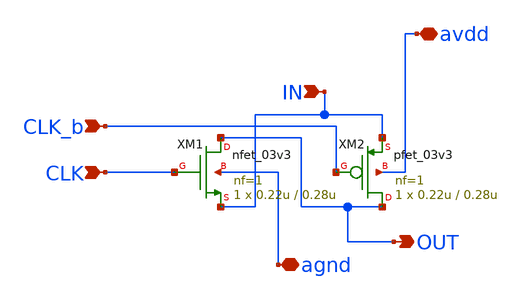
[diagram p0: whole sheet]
** sch_path: mpw18h1/cisar-gen/xschem/TBD/transimission_gate.sch
**.subckt transimission_gate IN OUT avdd agnd CLK_b CLK
*.ipin IN
*.opin OUT
*.iopin avdd
*.iopin agnd
*.ipin CLK_b
*.ipin CLK
XM1 OUT CLK IN agnd nfet_03v3 L=0.28u W=0.22u nf=1 ad='int((nf+1)/2) * W/nf * 0.18u' as='int((nf+2)/2) * W/nf * 0.18u'
+ pd='2*int((nf+1)/2) * (W/nf + 0.18u)' ps='2*int((nf+2)/2) * (W/nf + 0.18u)' nrd='0.18u / W' nrs='0.18u / W'
+ sa=0 sb=0 sd=0 m=1
XM2 OUT CLK_b IN avdd pfet_03v3 L=0.28u W=0.22u nf=1 ad='int((nf+1)/2) * W/nf * 0.18u' as='int((nf+2)/2) * W/nf * 0.18u'
+ pd='2*int((nf+1)/2) * (W/nf + 0.18u)' ps='2*int((nf+2)/2) * (W/nf + 0.18u)' nrd='0.18u / W' nrs='0.18u / W'
+ sa=0 sb=0 sd=0 m=1
**.ends
.end
